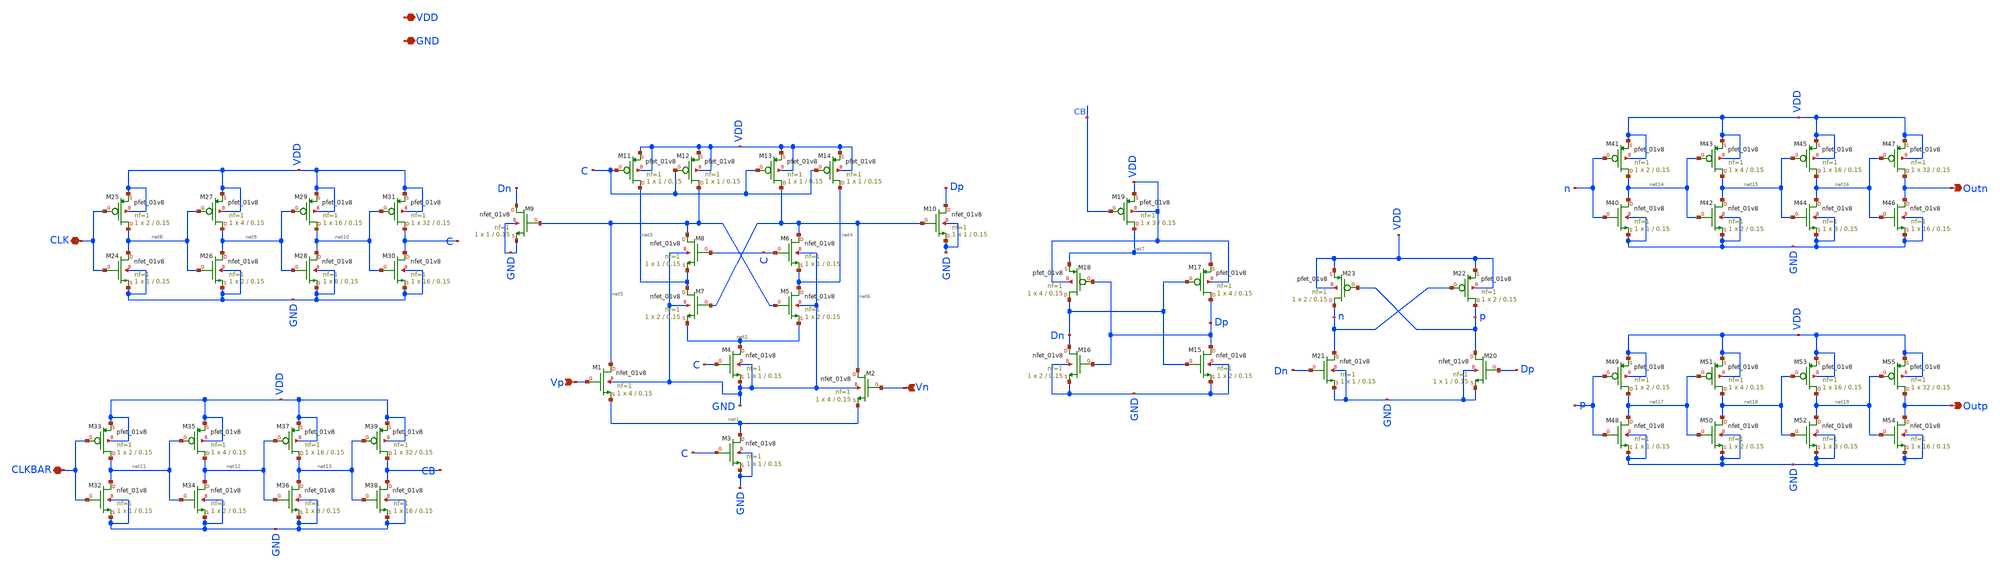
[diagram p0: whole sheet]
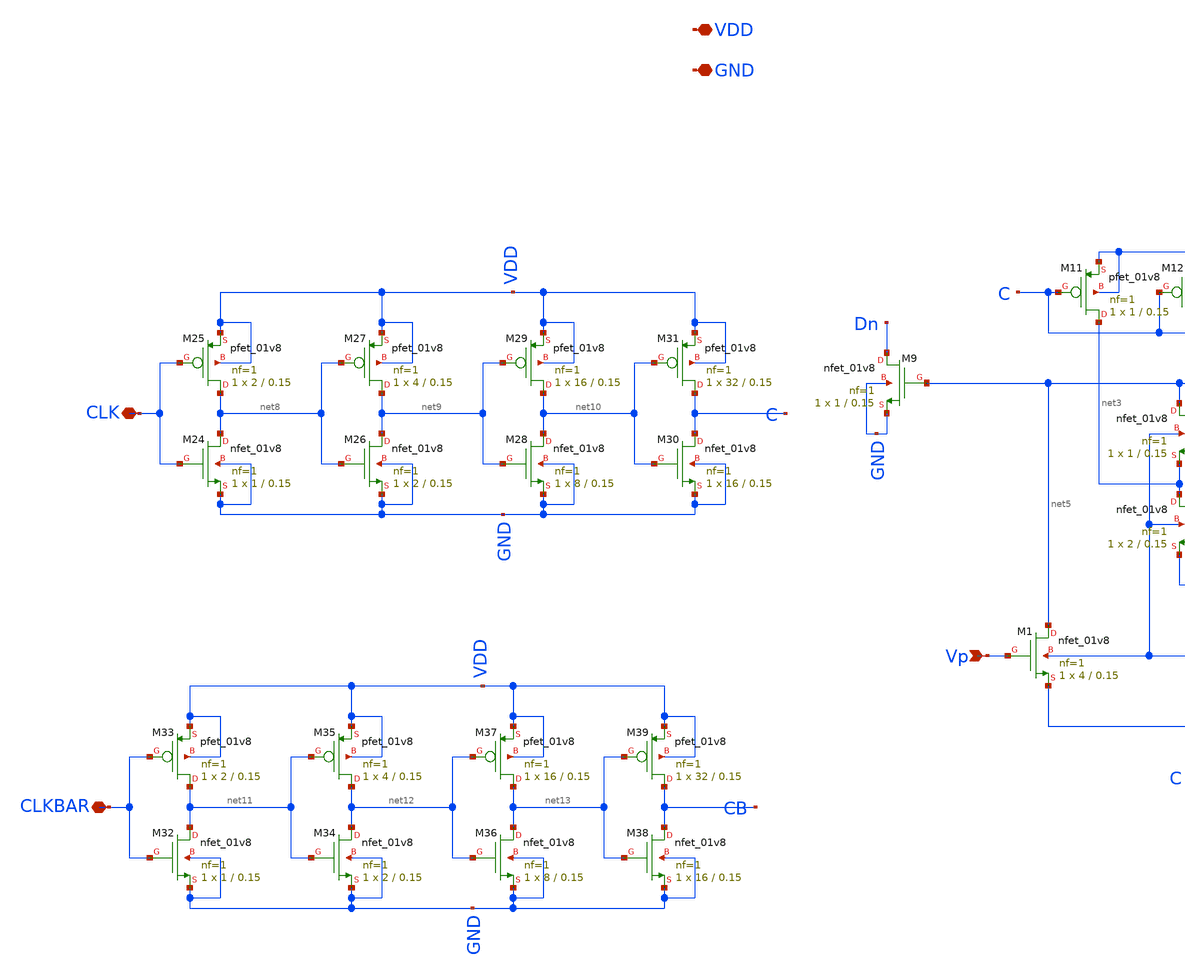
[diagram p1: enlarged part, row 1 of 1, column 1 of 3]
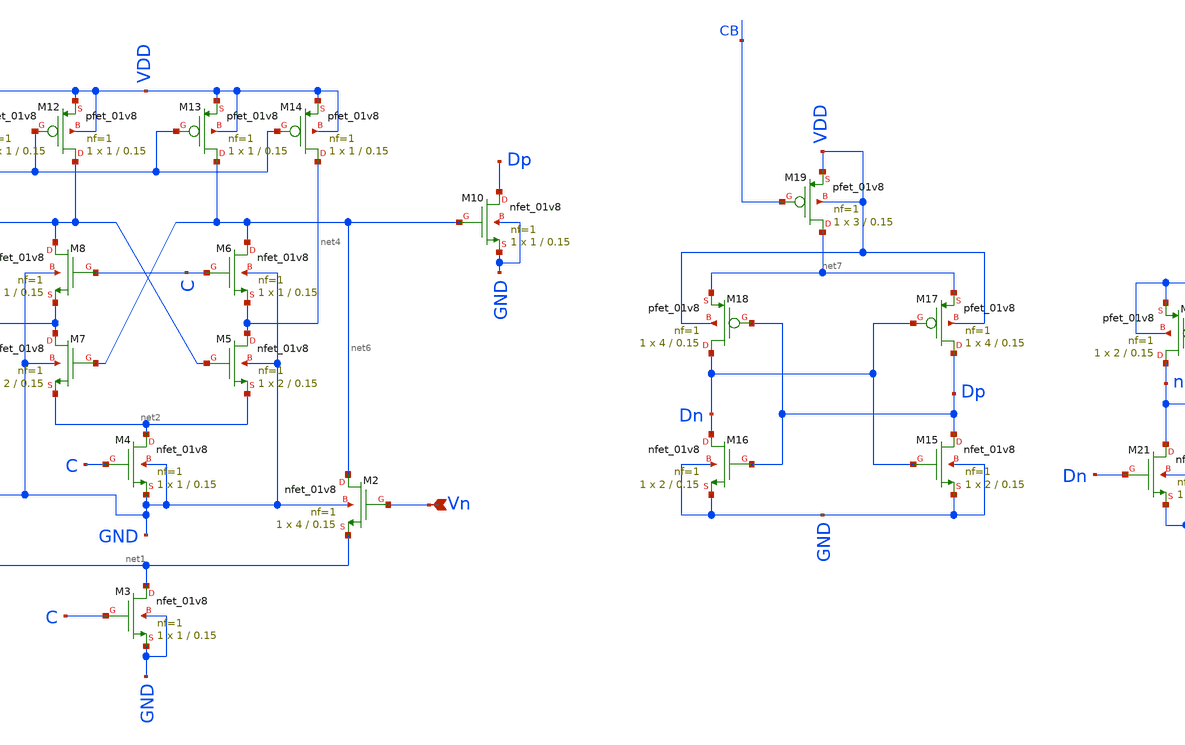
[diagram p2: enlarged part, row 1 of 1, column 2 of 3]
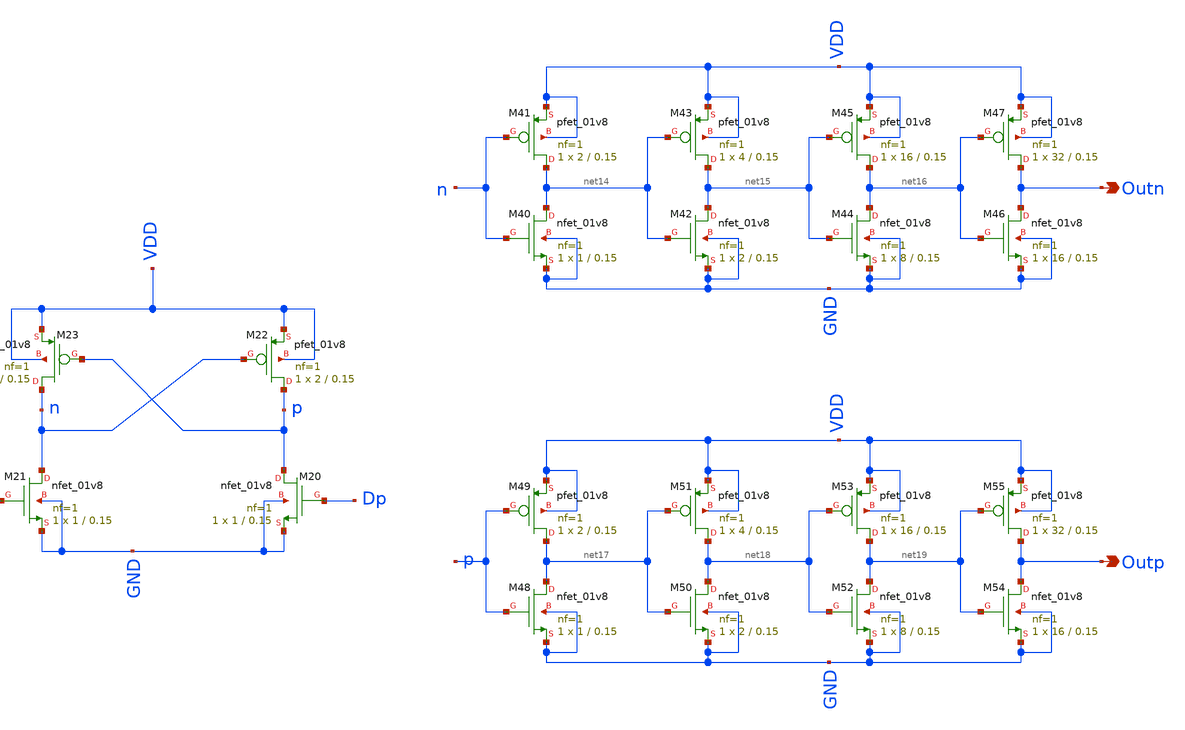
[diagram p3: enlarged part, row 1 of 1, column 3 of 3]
** sch_path: xschem/comparator.sch
**.subckt comparator VDD GND Vn Vp CLK Outn Outp CLKBAR
*.iopin VDD
*.iopin GND
*.ipin Vn
*.ipin Vp
*.iopin CLK
*.opin Outn
*.opin Outp
*.iopin CLKBAR
XM1 net5 Vp net1 GND sky130_fd_pr__nfet_01v8 L=0.15 W=4 nf=1 ad='int((nf+1)/2) * W/nf * 0.29' as='int((nf+2)/2) * W/nf * 0.29'
+ pd='2*int((nf+1)/2) * (W/nf + 0.29)' ps='2*int((nf+2)/2) * (W/nf + 0.29)' nrd='0.29 / W' nrs='0.29 / W'
+ sa=0 sb=0 sd=0 mult=1 m=1
XM2 net6 Vn net1 GND sky130_fd_pr__nfet_01v8 L=0.15 W=4 nf=1 ad='int((nf+1)/2) * W/nf * 0.29' as='int((nf+2)/2) * W/nf * 0.29'
+ pd='2*int((nf+1)/2) * (W/nf + 0.29)' ps='2*int((nf+2)/2) * (W/nf + 0.29)' nrd='0.29 / W' nrs='0.29 / W'
+ sa=0 sb=0 sd=0 mult=1 m=1
XM3 net1 C GND GND sky130_fd_pr__nfet_01v8 L=0.15 W=1 nf=1 ad='int((nf+1)/2) * W/nf * 0.29' as='int((nf+2)/2) * W/nf * 0.29'
+ pd='2*int((nf+1)/2) * (W/nf + 0.29)' ps='2*int((nf+2)/2) * (W/nf + 0.29)' nrd='0.29 / W' nrs='0.29 / W'
+ sa=0 sb=0 sd=0 mult=1 m=1
XM4 net2 C GND GND sky130_fd_pr__nfet_01v8 L=0.15 W=1 nf=1 ad='int((nf+1)/2) * W/nf * 0.29' as='int((nf+2)/2) * W/nf * 0.29'
+ pd='2*int((nf+1)/2) * (W/nf + 0.29)' ps='2*int((nf+2)/2) * (W/nf + 0.29)' nrd='0.29 / W' nrs='0.29 / W'
+ sa=0 sb=0 sd=0 mult=1 m=1
XM5 net4 net5 net2 GND sky130_fd_pr__nfet_01v8 L=0.15 W=2 nf=1 ad='int((nf+1)/2) * W/nf * 0.29' as='int((nf+2)/2) * W/nf * 0.29'
+ pd='2*int((nf+1)/2) * (W/nf + 0.29)' ps='2*int((nf+2)/2) * (W/nf + 0.29)' nrd='0.29 / W' nrs='0.29 / W'
+ sa=0 sb=0 sd=0 mult=1 m=1
XM6 net6 C net4 GND sky130_fd_pr__nfet_01v8 L=0.15 W=1 nf=1 ad='int((nf+1)/2) * W/nf * 0.29' as='int((nf+2)/2) * W/nf * 0.29'
+ pd='2*int((nf+1)/2) * (W/nf + 0.29)' ps='2*int((nf+2)/2) * (W/nf + 0.29)' nrd='0.29 / W' nrs='0.29 / W'
+ sa=0 sb=0 sd=0 mult=1 m=1
XM7 net3 net6 net2 GND sky130_fd_pr__nfet_01v8 L=0.15 W=2 nf=1 ad='int((nf+1)/2) * W/nf * 0.29' as='int((nf+2)/2) * W/nf * 0.29'
+ pd='2*int((nf+1)/2) * (W/nf + 0.29)' ps='2*int((nf+2)/2) * (W/nf + 0.29)' nrd='0.29 / W' nrs='0.29 / W'
+ sa=0 sb=0 sd=0 mult=1 m=1
XM8 net5 C net3 GND sky130_fd_pr__nfet_01v8 L=0.15 W=1 nf=1 ad='int((nf+1)/2) * W/nf * 0.29' as='int((nf+2)/2) * W/nf * 0.29'
+ pd='2*int((nf+1)/2) * (W/nf + 0.29)' ps='2*int((nf+2)/2) * (W/nf + 0.29)' nrd='0.29 / W' nrs='0.29 / W'
+ sa=0 sb=0 sd=0 mult=1 m=1
XM9 Dn net5 GND GND sky130_fd_pr__nfet_01v8 L=0.15 W=1 nf=1 ad='int((nf+1)/2) * W/nf * 0.29' as='int((nf+2)/2) * W/nf * 0.29'
+ pd='2*int((nf+1)/2) * (W/nf + 0.29)' ps='2*int((nf+2)/2) * (W/nf + 0.29)' nrd='0.29 / W' nrs='0.29 / W'
+ sa=0 sb=0 sd=0 mult=1 m=1
XM10 Dp net6 GND GND sky130_fd_pr__nfet_01v8 L=0.15 W=1 nf=1 ad='int((nf+1)/2) * W/nf * 0.29' as='int((nf+2)/2) * W/nf * 0.29'
+ pd='2*int((nf+1)/2) * (W/nf + 0.29)' ps='2*int((nf+2)/2) * (W/nf + 0.29)' nrd='0.29 / W' nrs='0.29 / W'
+ sa=0 sb=0 sd=0 mult=1 m=1
XM11 net3 C VDD VDD sky130_fd_pr__pfet_01v8 L=0.15 W=1 nf=1 ad='int((nf+1)/2) * W/nf * 0.29' as='int((nf+2)/2) * W/nf * 0.29'
+ pd='2*int((nf+1)/2) * (W/nf + 0.29)' ps='2*int((nf+2)/2) * (W/nf + 0.29)' nrd='0.29 / W' nrs='0.29 / W'
+ sa=0 sb=0 sd=0 mult=1 m=1
XM12 net5 C VDD VDD sky130_fd_pr__pfet_01v8 L=0.15 W=1 nf=1 ad='int((nf+1)/2) * W/nf * 0.29' as='int((nf+2)/2) * W/nf * 0.29'
+ pd='2*int((nf+1)/2) * (W/nf + 0.29)' ps='2*int((nf+2)/2) * (W/nf + 0.29)' nrd='0.29 / W' nrs='0.29 / W'
+ sa=0 sb=0 sd=0 mult=1 m=1
XM13 net6 C VDD VDD sky130_fd_pr__pfet_01v8 L=0.15 W=1 nf=1 ad='int((nf+1)/2) * W/nf * 0.29' as='int((nf+2)/2) * W/nf * 0.29'
+ pd='2*int((nf+1)/2) * (W/nf + 0.29)' ps='2*int((nf+2)/2) * (W/nf + 0.29)' nrd='0.29 / W' nrs='0.29 / W'
+ sa=0 sb=0 sd=0 mult=1 m=1
XM14 net4 C VDD VDD sky130_fd_pr__pfet_01v8 L=0.15 W=1 nf=1 ad='int((nf+1)/2) * W/nf * 0.29' as='int((nf+2)/2) * W/nf * 0.29'
+ pd='2*int((nf+1)/2) * (W/nf + 0.29)' ps='2*int((nf+2)/2) * (W/nf + 0.29)' nrd='0.29 / W' nrs='0.29 / W'
+ sa=0 sb=0 sd=0 mult=1 m=1
XM15 Dp Dn GND GND sky130_fd_pr__nfet_01v8 L=0.15 W=2 nf=1 ad='int((nf+1)/2) * W/nf * 0.29' as='int((nf+2)/2) * W/nf * 0.29'
+ pd='2*int((nf+1)/2) * (W/nf + 0.29)' ps='2*int((nf+2)/2) * (W/nf + 0.29)' nrd='0.29 / W' nrs='0.29 / W'
+ sa=0 sb=0 sd=0 mult=1 m=1
XM16 Dn Dp GND GND sky130_fd_pr__nfet_01v8 L=0.15 W=2 nf=1 ad='int((nf+1)/2) * W/nf * 0.29' as='int((nf+2)/2) * W/nf * 0.29'
+ pd='2*int((nf+1)/2) * (W/nf + 0.29)' ps='2*int((nf+2)/2) * (W/nf + 0.29)' nrd='0.29 / W' nrs='0.29 / W'
+ sa=0 sb=0 sd=0 mult=1 m=1
XM17 Dp Dn net7 VDD sky130_fd_pr__pfet_01v8 L=0.15 W=4 nf=1 ad='int((nf+1)/2) * W/nf * 0.29' as='int((nf+2)/2) * W/nf * 0.29'
+ pd='2*int((nf+1)/2) * (W/nf + 0.29)' ps='2*int((nf+2)/2) * (W/nf + 0.29)' nrd='0.29 / W' nrs='0.29 / W'
+ sa=0 sb=0 sd=0 mult=1 m=1
XM18 Dn Dp net7 VDD sky130_fd_pr__pfet_01v8 L=0.15 W=4 nf=1 ad='int((nf+1)/2) * W/nf * 0.29' as='int((nf+2)/2) * W/nf * 0.29'
+ pd='2*int((nf+1)/2) * (W/nf + 0.29)' ps='2*int((nf+2)/2) * (W/nf + 0.29)' nrd='0.29 / W' nrs='0.29 / W'
+ sa=0 sb=0 sd=0 mult=1 m=1
XM19 net7 CB VDD VDD sky130_fd_pr__pfet_01v8 L=0.15 W=3 nf=1 ad='int((nf+1)/2) * W/nf * 0.29' as='int((nf+2)/2) * W/nf * 0.29'
+ pd='2*int((nf+1)/2) * (W/nf + 0.29)' ps='2*int((nf+2)/2) * (W/nf + 0.29)' nrd='0.29 / W' nrs='0.29 / W'
+ sa=0 sb=0 sd=0 mult=1 m=1
XM20 p Dp GND GND sky130_fd_pr__nfet_01v8 L=0.15 W=1 nf=1 ad='int((nf+1)/2) * W/nf * 0.29' as='int((nf+2)/2) * W/nf * 0.29'
+ pd='2*int((nf+1)/2) * (W/nf + 0.29)' ps='2*int((nf+2)/2) * (W/nf + 0.29)' nrd='0.29 / W' nrs='0.29 / W'
+ sa=0 sb=0 sd=0 mult=1 m=1
XM21 n Dn GND GND sky130_fd_pr__nfet_01v8 L=0.15 W=1 nf=1 ad='int((nf+1)/2) * W/nf * 0.29' as='int((nf+2)/2) * W/nf * 0.29'
+ pd='2*int((nf+1)/2) * (W/nf + 0.29)' ps='2*int((nf+2)/2) * (W/nf + 0.29)' nrd='0.29 / W' nrs='0.29 / W'
+ sa=0 sb=0 sd=0 mult=1 m=1
XM22 p n VDD VDD sky130_fd_pr__pfet_01v8 L=0.15 W=2 nf=1 ad='int((nf+1)/2) * W/nf * 0.29' as='int((nf+2)/2) * W/nf * 0.29'
+ pd='2*int((nf+1)/2) * (W/nf + 0.29)' ps='2*int((nf+2)/2) * (W/nf + 0.29)' nrd='0.29 / W' nrs='0.29 / W'
+ sa=0 sb=0 sd=0 mult=1 m=1
XM23 n p VDD VDD sky130_fd_pr__pfet_01v8 L=0.15 W=2 nf=1 ad='int((nf+1)/2) * W/nf * 0.29' as='int((nf+2)/2) * W/nf * 0.29'
+ pd='2*int((nf+1)/2) * (W/nf + 0.29)' ps='2*int((nf+2)/2) * (W/nf + 0.29)' nrd='0.29 / W' nrs='0.29 / W'
+ sa=0 sb=0 sd=0 mult=1 m=1
XM24 net8 CLK GND GND sky130_fd_pr__nfet_01v8 L=0.15 W=1 nf=1 ad='int((nf+1)/2) * W/nf * 0.29' as='int((nf+2)/2) * W/nf * 0.29'
+ pd='2*int((nf+1)/2) * (W/nf + 0.29)' ps='2*int((nf+2)/2) * (W/nf + 0.29)' nrd='0.29 / W' nrs='0.29 / W'
+ sa=0 sb=0 sd=0 mult=1 m=1
XM25 net8 CLK VDD VDD sky130_fd_pr__pfet_01v8 L=0.15 W=2 nf=1 ad='int((nf+1)/2) * W/nf * 0.29' as='int((nf+2)/2) * W/nf * 0.29'
+ pd='2*int((nf+1)/2) * (W/nf + 0.29)' ps='2*int((nf+2)/2) * (W/nf + 0.29)' nrd='0.29 / W' nrs='0.29 / W'
+ sa=0 sb=0 sd=0 mult=1 m=1
XM26 net9 net8 GND GND sky130_fd_pr__nfet_01v8 L=0.15 W=2 nf=1 ad='int((nf+1)/2) * W/nf * 0.29' as='int((nf+2)/2) * W/nf * 0.29'
+ pd='2*int((nf+1)/2) * (W/nf + 0.29)' ps='2*int((nf+2)/2) * (W/nf + 0.29)' nrd='0.29 / W' nrs='0.29 / W'
+ sa=0 sb=0 sd=0 mult=1 m=1
XM27 net9 net8 VDD VDD sky130_fd_pr__pfet_01v8 L=0.15 W=4 nf=1 ad='int((nf+1)/2) * W/nf * 0.29' as='int((nf+2)/2) * W/nf * 0.29'
+ pd='2*int((nf+1)/2) * (W/nf + 0.29)' ps='2*int((nf+2)/2) * (W/nf + 0.29)' nrd='0.29 / W' nrs='0.29 / W'
+ sa=0 sb=0 sd=0 mult=1 m=1
XM28 net10 net9 GND GND sky130_fd_pr__nfet_01v8 L=0.15 W=8 nf=1 ad='int((nf+1)/2) * W/nf * 0.29' as='int((nf+2)/2) * W/nf * 0.29'
+ pd='2*int((nf+1)/2) * (W/nf + 0.29)' ps='2*int((nf+2)/2) * (W/nf + 0.29)' nrd='0.29 / W' nrs='0.29 / W'
+ sa=0 sb=0 sd=0 mult=1 m=1
XM29 net10 net9 VDD VDD sky130_fd_pr__pfet_01v8 L=0.15 W=16 nf=1 ad='int((nf+1)/2) * W/nf * 0.29' as='int((nf+2)/2) * W/nf * 0.29'
+ pd='2*int((nf+1)/2) * (W/nf + 0.29)' ps='2*int((nf+2)/2) * (W/nf + 0.29)' nrd='0.29 / W' nrs='0.29 / W'
+ sa=0 sb=0 sd=0 mult=1 m=1
XM30 C net10 GND GND sky130_fd_pr__nfet_01v8 L=0.15 W=16 nf=1 ad='int((nf+1)/2) * W/nf * 0.29' as='int((nf+2)/2) * W/nf * 0.29'
+ pd='2*int((nf+1)/2) * (W/nf + 0.29)' ps='2*int((nf+2)/2) * (W/nf + 0.29)' nrd='0.29 / W' nrs='0.29 / W'
+ sa=0 sb=0 sd=0 mult=1 m=1
XM31 C net10 VDD VDD sky130_fd_pr__pfet_01v8 L=0.15 W=32 nf=1 ad='int((nf+1)/2) * W/nf * 0.29' as='int((nf+2)/2) * W/nf * 0.29'
+ pd='2*int((nf+1)/2) * (W/nf + 0.29)' ps='2*int((nf+2)/2) * (W/nf + 0.29)' nrd='0.29 / W' nrs='0.29 / W'
+ sa=0 sb=0 sd=0 mult=1 m=1
XM32 net11 CLKBAR GND GND sky130_fd_pr__nfet_01v8 L=0.15 W=1 nf=1 ad='int((nf+1)/2) * W/nf * 0.29' as='int((nf+2)/2) * W/nf * 0.29'
+ pd='2*int((nf+1)/2) * (W/nf + 0.29)' ps='2*int((nf+2)/2) * (W/nf + 0.29)' nrd='0.29 / W' nrs='0.29 / W'
+ sa=0 sb=0 sd=0 mult=1 m=1
XM33 net11 CLKBAR VDD VDD sky130_fd_pr__pfet_01v8 L=0.15 W=2 nf=1 ad='int((nf+1)/2) * W/nf * 0.29' as='int((nf+2)/2) * W/nf * 0.29'
+ pd='2*int((nf+1)/2) * (W/nf + 0.29)' ps='2*int((nf+2)/2) * (W/nf + 0.29)' nrd='0.29 / W' nrs='0.29 / W'
+ sa=0 sb=0 sd=0 mult=1 m=1
XM34 net12 net11 GND GND sky130_fd_pr__nfet_01v8 L=0.15 W=2 nf=1 ad='int((nf+1)/2) * W/nf * 0.29' as='int((nf+2)/2) * W/nf * 0.29'
+ pd='2*int((nf+1)/2) * (W/nf + 0.29)' ps='2*int((nf+2)/2) * (W/nf + 0.29)' nrd='0.29 / W' nrs='0.29 / W'
+ sa=0 sb=0 sd=0 mult=1 m=1
XM35 net12 net11 VDD VDD sky130_fd_pr__pfet_01v8 L=0.15 W=4 nf=1 ad='int((nf+1)/2) * W/nf * 0.29' as='int((nf+2)/2) * W/nf * 0.29'
+ pd='2*int((nf+1)/2) * (W/nf + 0.29)' ps='2*int((nf+2)/2) * (W/nf + 0.29)' nrd='0.29 / W' nrs='0.29 / W'
+ sa=0 sb=0 sd=0 mult=1 m=1
XM36 net13 net12 GND GND sky130_fd_pr__nfet_01v8 L=0.15 W=8 nf=1 ad='int((nf+1)/2) * W/nf * 0.29' as='int((nf+2)/2) * W/nf * 0.29'
+ pd='2*int((nf+1)/2) * (W/nf + 0.29)' ps='2*int((nf+2)/2) * (W/nf + 0.29)' nrd='0.29 / W' nrs='0.29 / W'
+ sa=0 sb=0 sd=0 mult=1 m=1
XM37 net13 net12 VDD VDD sky130_fd_pr__pfet_01v8 L=0.15 W=16 nf=1 ad='int((nf+1)/2) * W/nf * 0.29' as='int((nf+2)/2) * W/nf * 0.29'
+ pd='2*int((nf+1)/2) * (W/nf + 0.29)' ps='2*int((nf+2)/2) * (W/nf + 0.29)' nrd='0.29 / W' nrs='0.29 / W'
+ sa=0 sb=0 sd=0 mult=1 m=1
XM38 CB net13 GND GND sky130_fd_pr__nfet_01v8 L=0.15 W=16 nf=1 ad='int((nf+1)/2) * W/nf * 0.29' as='int((nf+2)/2) * W/nf * 0.29'
+ pd='2*int((nf+1)/2) * (W/nf + 0.29)' ps='2*int((nf+2)/2) * (W/nf + 0.29)' nrd='0.29 / W' nrs='0.29 / W'
+ sa=0 sb=0 sd=0 mult=1 m=1
XM39 CB net13 VDD VDD sky130_fd_pr__pfet_01v8 L=0.15 W=32 nf=1 ad='int((nf+1)/2) * W/nf * 0.29' as='int((nf+2)/2) * W/nf * 0.29'
+ pd='2*int((nf+1)/2) * (W/nf + 0.29)' ps='2*int((nf+2)/2) * (W/nf + 0.29)' nrd='0.29 / W' nrs='0.29 / W'
+ sa=0 sb=0 sd=0 mult=1 m=1
XM40 net14 n GND GND sky130_fd_pr__nfet_01v8 L=0.15 W=1 nf=1 ad='int((nf+1)/2) * W/nf * 0.29' as='int((nf+2)/2) * W/nf * 0.29'
+ pd='2*int((nf+1)/2) * (W/nf + 0.29)' ps='2*int((nf+2)/2) * (W/nf + 0.29)' nrd='0.29 / W' nrs='0.29 / W'
+ sa=0 sb=0 sd=0 mult=1 m=1
XM41 net14 n VDD VDD sky130_fd_pr__pfet_01v8 L=0.15 W=2 nf=1 ad='int((nf+1)/2) * W/nf * 0.29' as='int((nf+2)/2) * W/nf * 0.29'
+ pd='2*int((nf+1)/2) * (W/nf + 0.29)' ps='2*int((nf+2)/2) * (W/nf + 0.29)' nrd='0.29 / W' nrs='0.29 / W'
+ sa=0 sb=0 sd=0 mult=1 m=1
XM42 net15 net14 GND GND sky130_fd_pr__nfet_01v8 L=0.15 W=2 nf=1 ad='int((nf+1)/2) * W/nf * 0.29' as='int((nf+2)/2) * W/nf * 0.29'
+ pd='2*int((nf+1)/2) * (W/nf + 0.29)' ps='2*int((nf+2)/2) * (W/nf + 0.29)' nrd='0.29 / W' nrs='0.29 / W'
+ sa=0 sb=0 sd=0 mult=1 m=1
XM43 net15 net14 VDD VDD sky130_fd_pr__pfet_01v8 L=0.15 W=4 nf=1 ad='int((nf+1)/2) * W/nf * 0.29' as='int((nf+2)/2) * W/nf * 0.29'
+ pd='2*int((nf+1)/2) * (W/nf + 0.29)' ps='2*int((nf+2)/2) * (W/nf + 0.29)' nrd='0.29 / W' nrs='0.29 / W'
+ sa=0 sb=0 sd=0 mult=1 m=1
XM44 net16 net15 GND GND sky130_fd_pr__nfet_01v8 L=0.15 W=8 nf=1 ad='int((nf+1)/2) * W/nf * 0.29' as='int((nf+2)/2) * W/nf * 0.29'
+ pd='2*int((nf+1)/2) * (W/nf + 0.29)' ps='2*int((nf+2)/2) * (W/nf + 0.29)' nrd='0.29 / W' nrs='0.29 / W'
+ sa=0 sb=0 sd=0 mult=1 m=1
XM45 net16 net15 VDD VDD sky130_fd_pr__pfet_01v8 L=0.15 W=16 nf=1 ad='int((nf+1)/2) * W/nf * 0.29' as='int((nf+2)/2) * W/nf * 0.29'
+ pd='2*int((nf+1)/2) * (W/nf + 0.29)' ps='2*int((nf+2)/2) * (W/nf + 0.29)' nrd='0.29 / W' nrs='0.29 / W'
+ sa=0 sb=0 sd=0 mult=1 m=1
XM46 Outn net16 GND GND sky130_fd_pr__nfet_01v8 L=0.15 W=16 nf=1 ad='int((nf+1)/2) * W/nf * 0.29' as='int((nf+2)/2) * W/nf * 0.29'
+ pd='2*int((nf+1)/2) * (W/nf + 0.29)' ps='2*int((nf+2)/2) * (W/nf + 0.29)' nrd='0.29 / W' nrs='0.29 / W'
+ sa=0 sb=0 sd=0 mult=1 m=1
XM47 Outn net16 VDD VDD sky130_fd_pr__pfet_01v8 L=0.15 W=32 nf=1 ad='int((nf+1)/2) * W/nf * 0.29' as='int((nf+2)/2) * W/nf * 0.29'
+ pd='2*int((nf+1)/2) * (W/nf + 0.29)' ps='2*int((nf+2)/2) * (W/nf + 0.29)' nrd='0.29 / W' nrs='0.29 / W'
+ sa=0 sb=0 sd=0 mult=1 m=1
XM48 net17 p GND GND sky130_fd_pr__nfet_01v8 L=0.15 W=1 nf=1 ad='int((nf+1)/2) * W/nf * 0.29' as='int((nf+2)/2) * W/nf * 0.29'
+ pd='2*int((nf+1)/2) * (W/nf + 0.29)' ps='2*int((nf+2)/2) * (W/nf + 0.29)' nrd='0.29 / W' nrs='0.29 / W'
+ sa=0 sb=0 sd=0 mult=1 m=1
XM49 net17 p VDD VDD sky130_fd_pr__pfet_01v8 L=0.15 W=2 nf=1 ad='int((nf+1)/2) * W/nf * 0.29' as='int((nf+2)/2) * W/nf * 0.29'
+ pd='2*int((nf+1)/2) * (W/nf + 0.29)' ps='2*int((nf+2)/2) * (W/nf + 0.29)' nrd='0.29 / W' nrs='0.29 / W'
+ sa=0 sb=0 sd=0 mult=1 m=1
XM50 net18 net17 GND GND sky130_fd_pr__nfet_01v8 L=0.15 W=2 nf=1 ad='int((nf+1)/2) * W/nf * 0.29' as='int((nf+2)/2) * W/nf * 0.29'
+ pd='2*int((nf+1)/2) * (W/nf + 0.29)' ps='2*int((nf+2)/2) * (W/nf + 0.29)' nrd='0.29 / W' nrs='0.29 / W'
+ sa=0 sb=0 sd=0 mult=1 m=1
XM51 net18 net17 VDD VDD sky130_fd_pr__pfet_01v8 L=0.15 W=4 nf=1 ad='int((nf+1)/2) * W/nf * 0.29' as='int((nf+2)/2) * W/nf * 0.29'
+ pd='2*int((nf+1)/2) * (W/nf + 0.29)' ps='2*int((nf+2)/2) * (W/nf + 0.29)' nrd='0.29 / W' nrs='0.29 / W'
+ sa=0 sb=0 sd=0 mult=1 m=1
XM52 net19 net18 GND GND sky130_fd_pr__nfet_01v8 L=0.15 W=8 nf=1 ad='int((nf+1)/2) * W/nf * 0.29' as='int((nf+2)/2) * W/nf * 0.29'
+ pd='2*int((nf+1)/2) * (W/nf + 0.29)' ps='2*int((nf+2)/2) * (W/nf + 0.29)' nrd='0.29 / W' nrs='0.29 / W'
+ sa=0 sb=0 sd=0 mult=1 m=1
XM53 net19 net18 VDD VDD sky130_fd_pr__pfet_01v8 L=0.15 W=16 nf=1 ad='int((nf+1)/2) * W/nf * 0.29' as='int((nf+2)/2) * W/nf * 0.29'
+ pd='2*int((nf+1)/2) * (W/nf + 0.29)' ps='2*int((nf+2)/2) * (W/nf + 0.29)' nrd='0.29 / W' nrs='0.29 / W'
+ sa=0 sb=0 sd=0 mult=1 m=1
XM54 Outp net19 GND GND sky130_fd_pr__nfet_01v8 L=0.15 W=16 nf=1 ad='int((nf+1)/2) * W/nf * 0.29' as='int((nf+2)/2) * W/nf * 0.29'
+ pd='2*int((nf+1)/2) * (W/nf + 0.29)' ps='2*int((nf+2)/2) * (W/nf + 0.29)' nrd='0.29 / W' nrs='0.29 / W'
+ sa=0 sb=0 sd=0 mult=1 m=1
XM55 Outp net19 VDD VDD sky130_fd_pr__pfet_01v8 L=0.15 W=32 nf=1 ad='int((nf+1)/2) * W/nf * 0.29' as='int((nf+2)/2) * W/nf * 0.29'
+ pd='2*int((nf+1)/2) * (W/nf + 0.29)' ps='2*int((nf+2)/2) * (W/nf + 0.29)' nrd='0.29 / W' nrs='0.29 / W'
+ sa=0 sb=0 sd=0 mult=1 m=1
**.ends
.end
